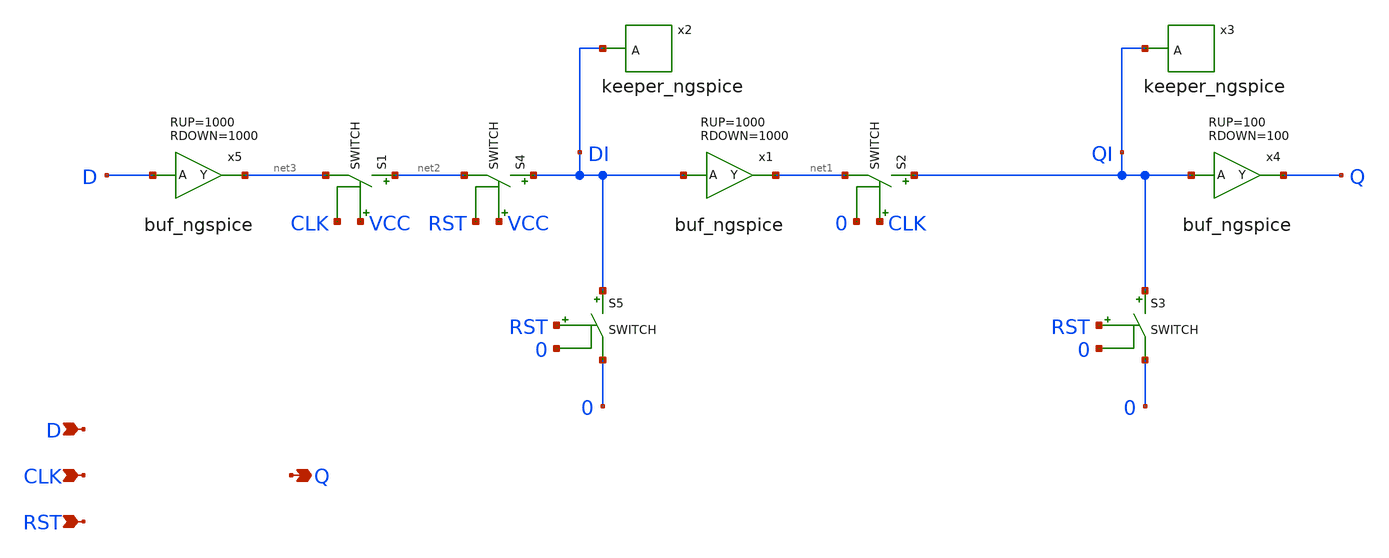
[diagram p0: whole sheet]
** sch_path: xschem-src/xschem_library/ngspice/flip_flop_ngspice.sch
* Copyright (C) 1998-2026 Stefan Frederik Schippers
* This program is free software; you can redistribute it and/or modify
* it under the terms of the GNU General Public License as published by
* the Free Software Foundation; either version 2 of the License, or
* (at your option) any later version.
* This program is distributed in the hope that it will be useful,
* but WITHOUT ANY WARRANTY; without even the implied warranty of
* MERCHANTABILITY or FITNESS FOR A PARTICULAR PURPOSE.  See the
* GNU General Public License for more details.
* You should have received a copy of the GNU General Public License
* along with this program; if not, write to the Free Software
**.subckt flip_flop_ngspice D CLK RST Q
*.ipin D
*.ipin CLK
*.ipin RST
*.opin Q
x2 DI keeper_ngspice
S1 net2 net3 VCC CLK SWITCH
S2 QI net1 CLK 0 SWITCH
x3 QI keeper_ngspice
x4 Q QI buf_ngspice RUP=100 RDOWN=100
S3 QI 0 RST 0 SWITCH
x1 net1 DI buf_ngspice RUP=1000 RDOWN=1000
S4 DI net2 VCC RST SWITCH
S5 DI 0 RST 0 SWITCH
x5 net3 D buf_ngspice RUP=1000 RDOWN=1000
**.ends

* expanding   symbol:  keeper_ngspice.sym # of pins=1
** sym_path: xschem-src/xschem_library/ngspice/keeper_ngspice.sym
** sch_path: xschem-src/xschem_library/ngspice/keeper_ngspice.sch
.subckt keeper_ngspice A
*.ipin A
x1 Y A inv_ngspice RUP=2000 RDOWN=1000
x2 A Y inv_ngspice RUP=300k RDOWN=200k
.ends


* expanding   symbol:  buf_ngspice.sym # of pins=2
** sym_path: xschem-src/xschem_library/ngspice/buf_ngspice.sym
** sch_path: xschem-src/xschem_library/ngspice/buf_ngspice.sch
.subckt buf_ngspice Y A  RUP=2000 RDOWN=1000
*.ipin A
*.opin Y
B1 X1 0 V = 'VCC/2*(1+tanh((V(A1)-VCC/2)*100))'
C3 Y1 0 8f m=1
C1 A1 0 4f m=1
V1 Y Y1 0
V2 A1 A 0
B2 X1 Y1 I = 'v(X1,Y1) > 0 ? v(X1,Y1) / RUP : v(X1,Y1) / RDOWN'
.ends


* expanding   symbol:  inv_ngspice.sym # of pins=2
** sym_path: xschem-src/xschem_library/ngspice/inv_ngspice.sym
** sch_path: xschem-src/xschem_library/ngspice/inv_ngspice.sch
.subckt inv_ngspice Y A  RUP=2000 RDOWN=1000
*.ipin A
*.opin Y
B1 X1 0 V = 'VCC/2*(1-tanh((V(A1)-VCC/2)*100))'
C1 A1 0 8f m=1
C2 Y1 0 8f m=1
V1 Y Y1 0
.save i(v1)
V2 A1 A 0
.save i(v2)
B2 X1 Y1 I = 'v(X1,Y1) > 0 ? v(X1,Y1) / RUP : v(X1,Y1) / RDOWN'
.ends

.end
